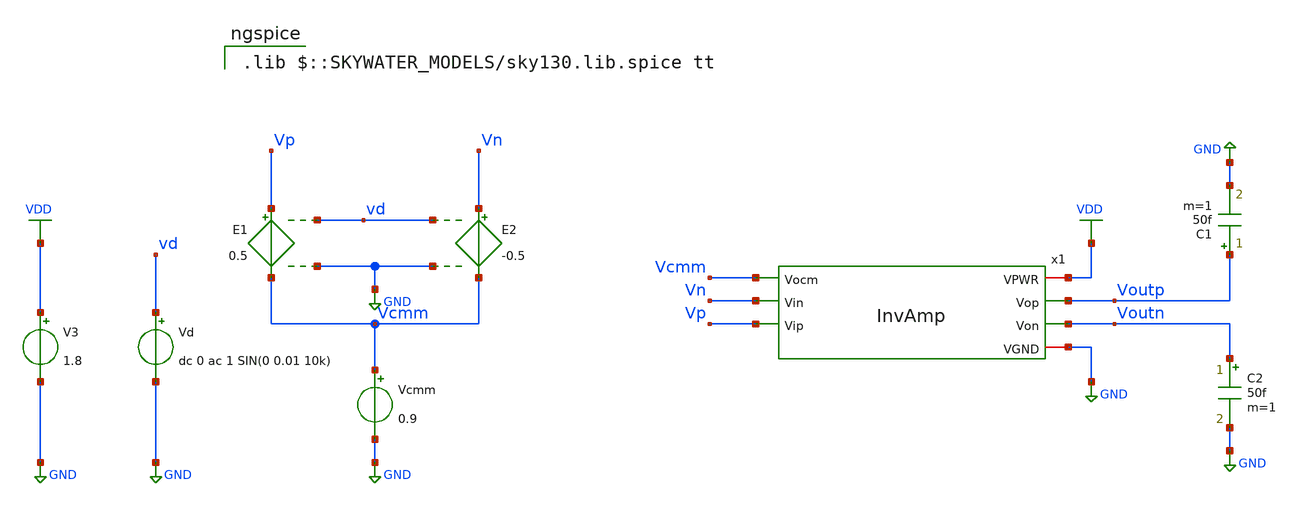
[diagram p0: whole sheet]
** sch_path: circuits/examples/InvAmp/InvAmp_tb.sch
**.subckt InvAmp_tb
V3 VDD GND 1.8
E1 Vp Vcmm vd GND 0.5
E2 Vn Vcmm vd GND -0.5
Vcmm Vcmm GND 0.9
Vd vd GND dc 0 ac 1 SIN(0 0.01 10k)
C2 Voutn GND 50f m=1
C1 Voutp GND 50f m=1
x1 VDD Vcmm Vn Voutp Voutn Vp GND InvAmp
**** begin user architecture code



* ngspice commands
.option savecurrents
.save all
.control
ac dec 1001 1 100Meg
let vod = V(Voutp)-V(Voutn)
meas ac gain max vod
let gain3dB = gain/sqrt(2)
meas ac BW TRIG at=1 TARG vod val=gain3dB fall=LAST
let GBW = BW*gain*1e-6
print GBW
print vodmax
plot vdb(vod) xlimit 1k 100Meg ylabel 'small signal gain'
let outd = 180/PI*cph(vod)
meas ac ftHz when vdb(vod)=1 fall=LAST
meas ac ph find outd when vdb(vod)=0 fall=LAST
let phm = ph+180
print phm
settype phase outd
plot outd xlimit 1k 100Meg ylabel 'phase'
tran 1u 1m
let vod = v(voutp)-v(voutn)
plot vod
op
.endc



 .lib $::SKYWATER_MODELS/sky130.lib.spice tt

**** end user architecture code
**.ends
.GLOBAL GND
.GLOBAL VDD
.end
